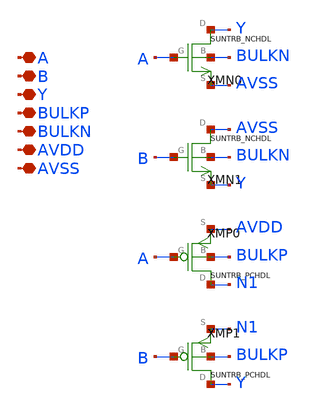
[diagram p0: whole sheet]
** sch_path: ip/sun_trb_sky130nm/design/SUN_TRB_SKY130NM/SUNTRB_NRX1_CV.sch
**.subckt SUNTRB_NRX1_CV A B Y BULKP BULKN AVDD AVSS
*.iopin A
*.iopin B
*.iopin Y
*.iopin BULKP
*.iopin BULKN
*.iopin AVDD
*.iopin AVSS
XMN0 Y A AVSS BULKN SUNTRB_NCHDL xoffset=0 yoffset=0 angle=0
XMN1 AVSS B Y BULKN SUNTRB_NCHDL xoffset=0 yoffset=0 angle=0
XMP0 N1 A AVDD BULKP SUNTRB_PCHDL
XMP1 Y B N1 BULKP SUNTRB_PCHDL
**.ends
.end
